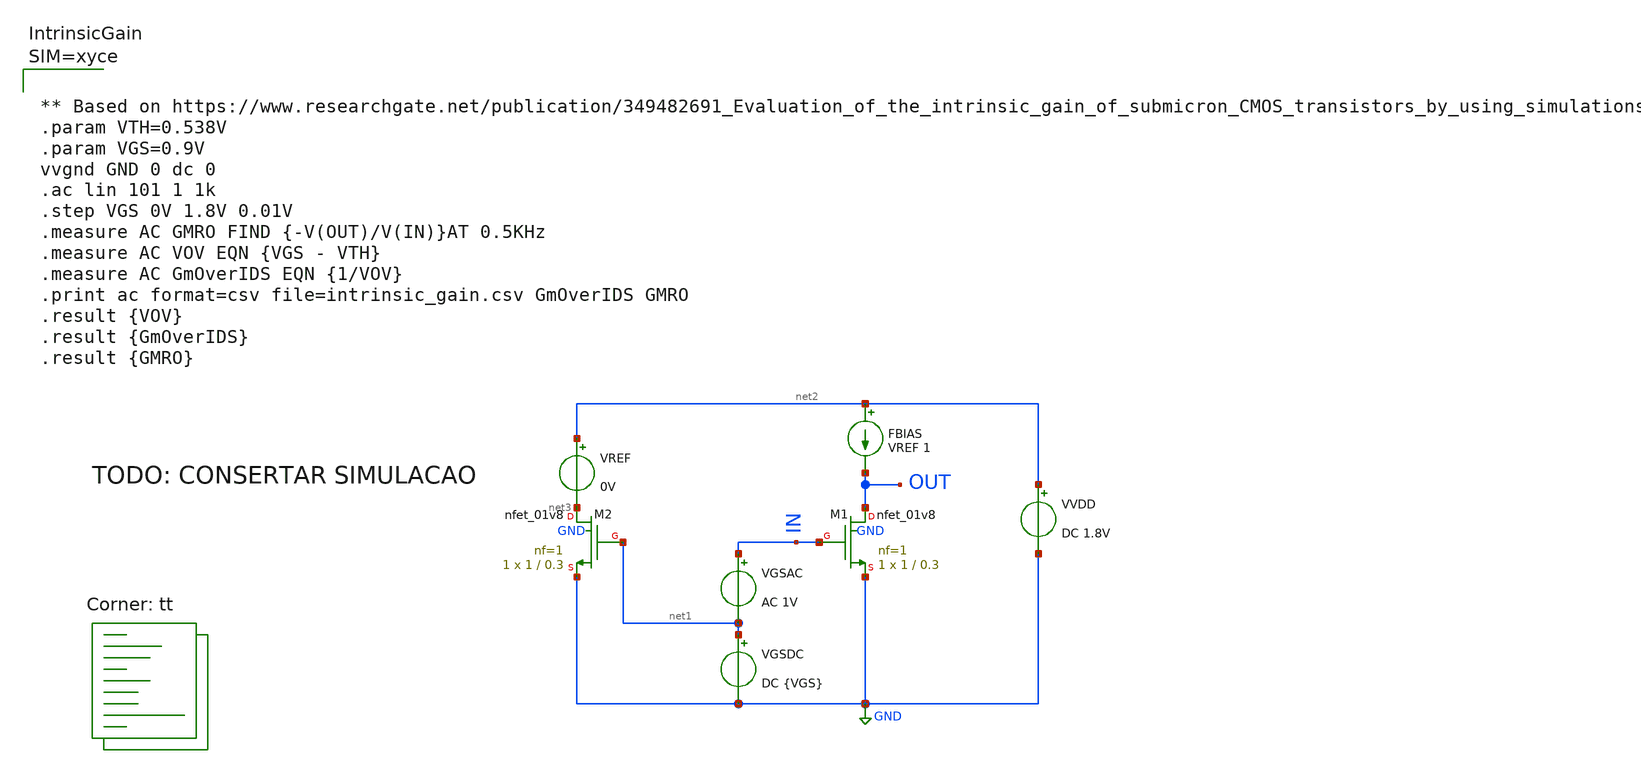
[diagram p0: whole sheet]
** sch_path: sky130/xschem/instrinsic-gain.sch
**.subckt instrinsic-gain
XM1 OUT IN GND GND sky130_fd_pr__nfet_01v8 L=0.3 W=1 nf=1 ad='int((nf+1)/2) * W/nf * 0.29' as='int((nf+2)/2) * W/nf * 0.29'
+ pd='2*int((nf+1)/2) * (W/nf + 0.29)' ps='2*int((nf+2)/2) * (W/nf + 0.29)' nrd='0.29 / W' nrs='0.29 / W'
+ sa=0 sb=0 sd=0 mult=1 m=1
VGSAC IN net1 AC 1V
FBIAS net2 OUT VREF 1
VVDD net2 GND DC 1.8V
VGSDC net1 GND DC {VGS}
XM2 net3 net1 GND GND sky130_fd_pr__nfet_01v8 L=0.3 W=1 nf=1 ad='int((nf+1)/2) * W/nf * 0.29' as='int((nf+2)/2) * W/nf * 0.29'
+ pd='2*int((nf+1)/2) * (W/nf + 0.29)' ps='2*int((nf+2)/2) * (W/nf + 0.29)' nrd='0.29 / W' nrs='0.29 / W'
+ sa=0 sb=0 sd=0 mult=1 m=1
VREF net2 net3 0V
**** begin user architecture code
.lib $::SKYWATER_MODELS/sky130.lib.spice tt



**** end user architecture code
**.ends
.GLOBAL GND
.end
